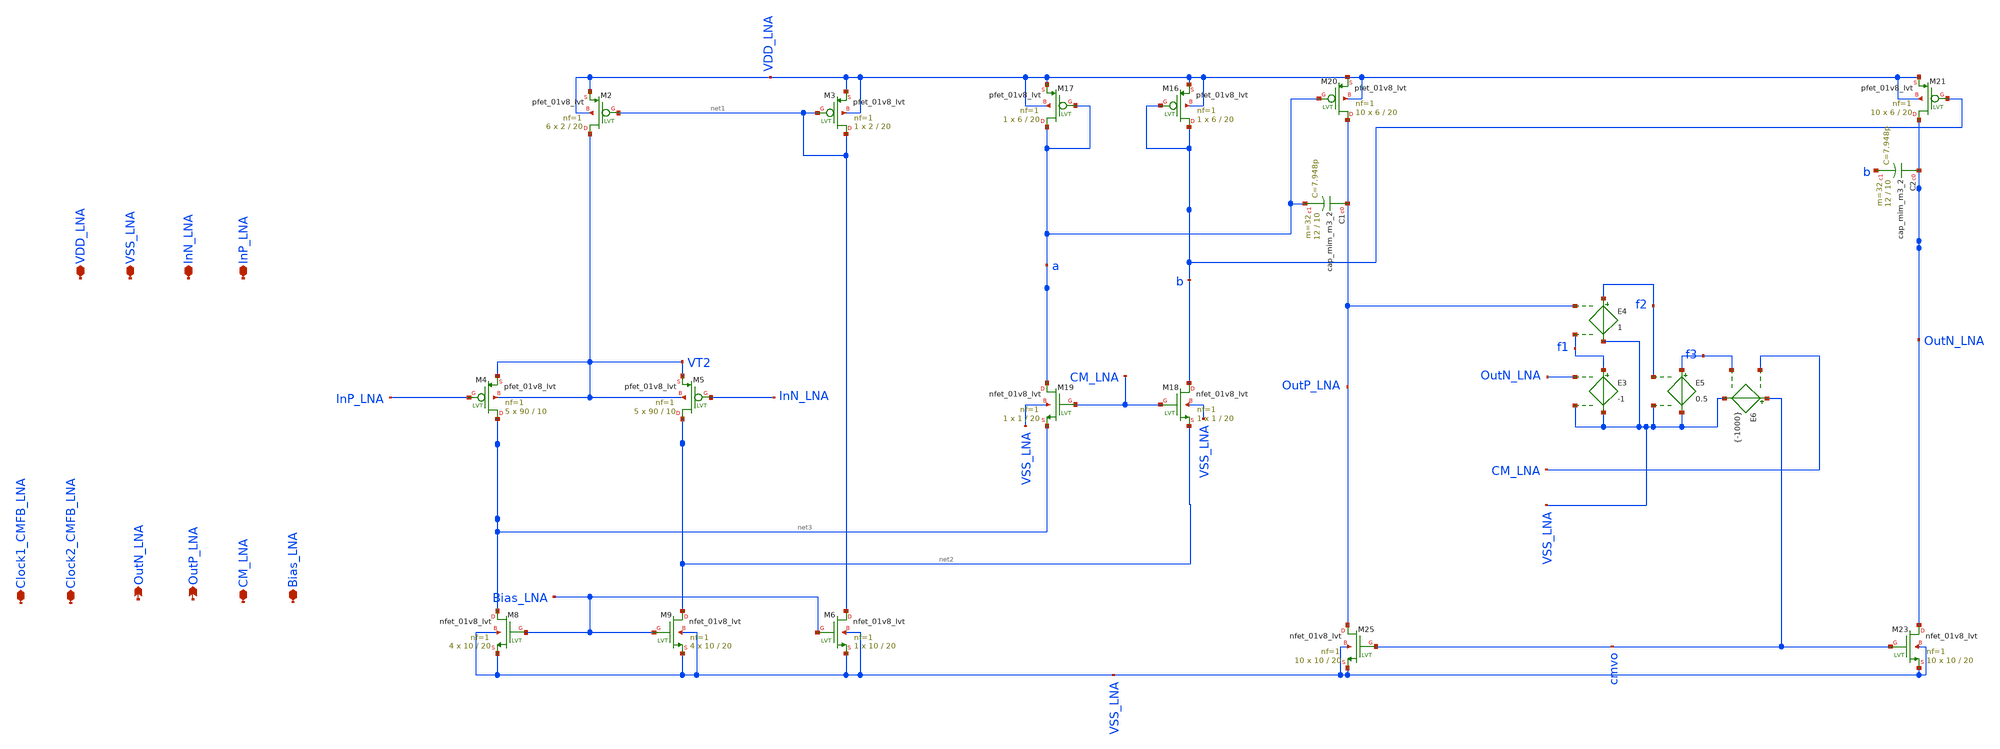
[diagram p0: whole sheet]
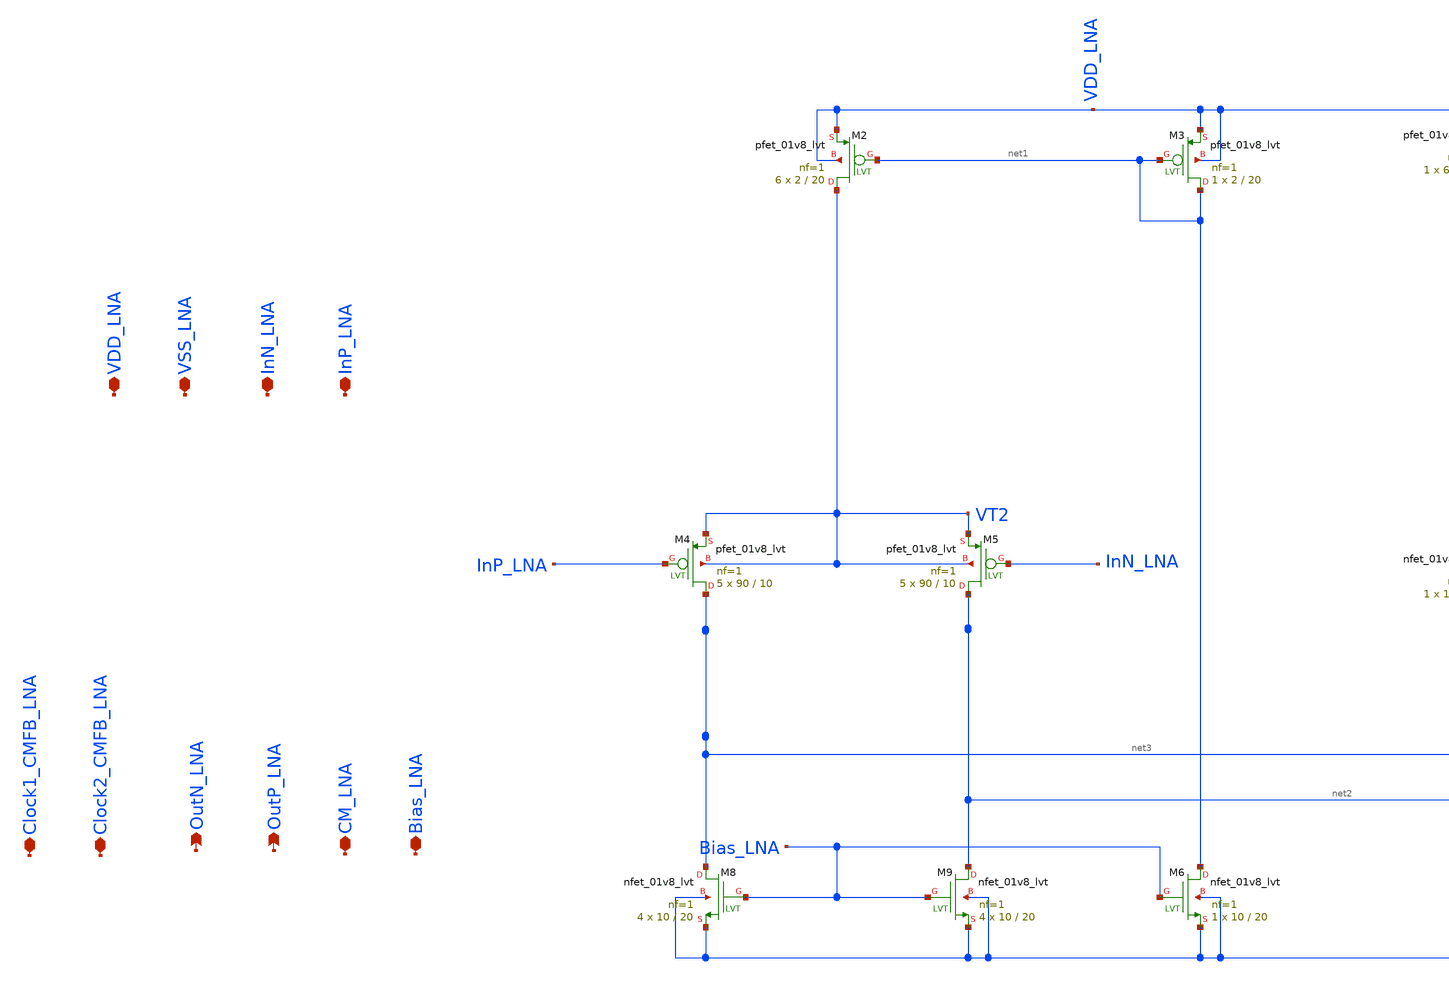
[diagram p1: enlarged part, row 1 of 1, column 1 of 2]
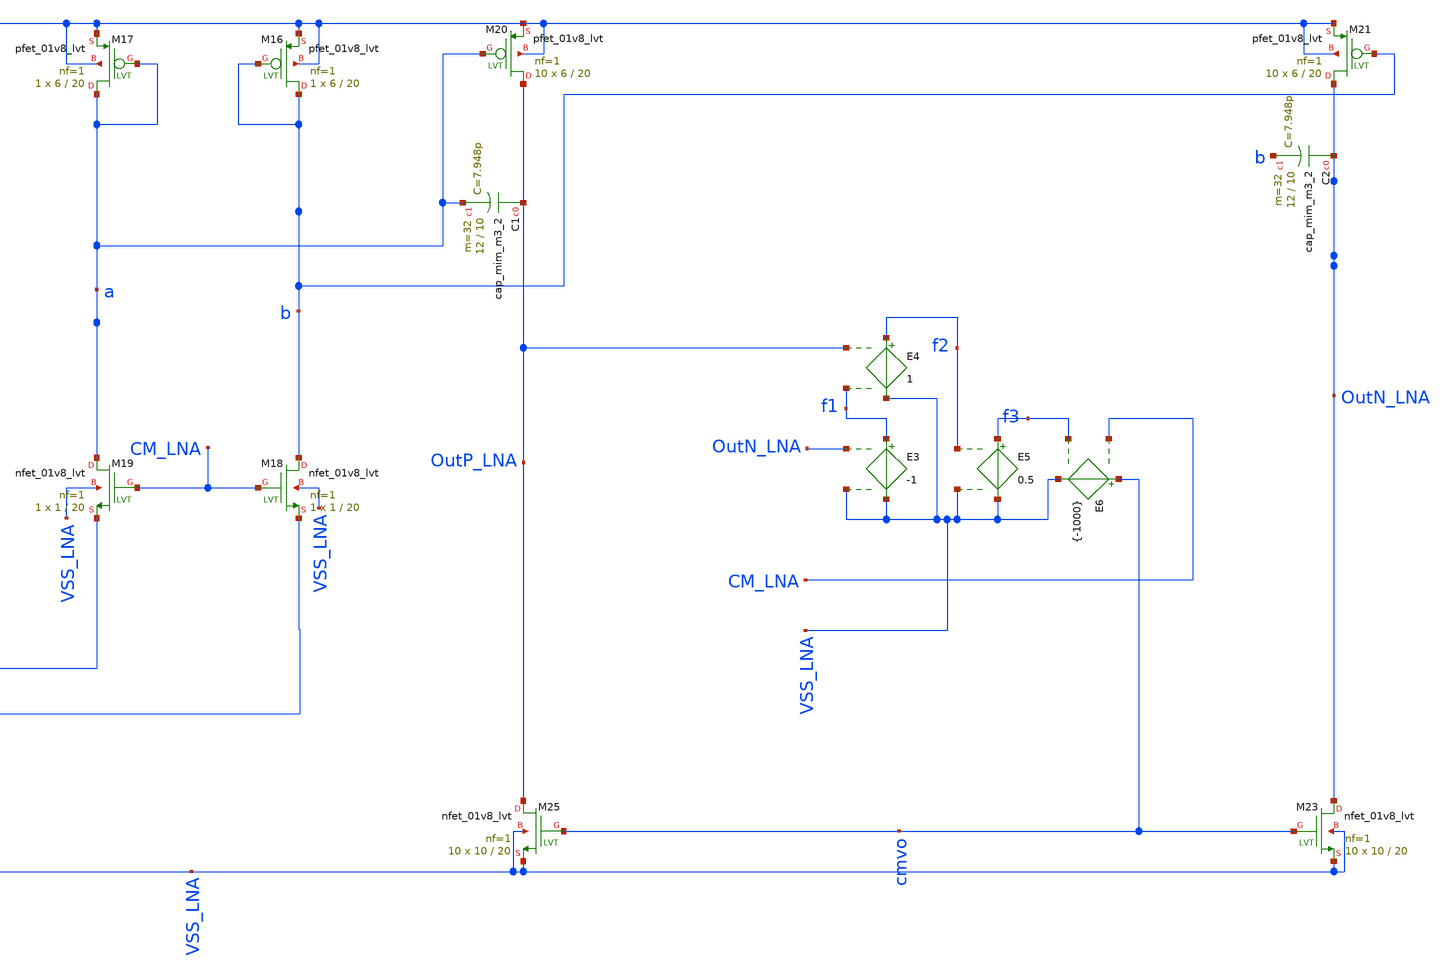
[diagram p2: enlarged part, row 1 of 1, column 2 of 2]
** sch_path: LNA_ac.sch
**.subckt LNA_ac InP_LNA InN_LNA VSS_LNA VDD_LNA CM_LNA OutP_LNA OutN_LNA Clock2_CMFB_LNA Bias_LNA
*+ Clock1_CMFB_LNA
*.iopin InP_LNA
*.iopin InN_LNA
*.iopin VSS_LNA
*.iopin VDD_LNA
*.iopin CM_LNA
*.opin OutP_LNA
*.opin OutN_LNA
*.iopin Clock2_CMFB_LNA
*.iopin Bias_LNA
*.iopin Clock1_CMFB_LNA
XM4 net3 InP_LNA VT2 VT2 sky130_fd_pr__pfet_01v8_lvt L=10 W=90 nf=1 ad='int((nf+1)/2) * W/nf * 0.29'
+ as='int((nf+2)/2) * W/nf * 0.29' pd='2*int((nf+1)/2) * (W/nf + 0.29)' ps='2*int((nf+2)/2) * (W/nf + 0.29)'
+ nrd='0.29 / W' nrs='0.29 / W' sa=0 sb=0 sd=0 mult=5 m=5
XM5 net2 InN_LNA VT2 VT2 sky130_fd_pr__pfet_01v8_lvt L=10 W=90 nf=1 ad='int((nf+1)/2) * W/nf * 0.29'
+ as='int((nf+2)/2) * W/nf * 0.29' pd='2*int((nf+1)/2) * (W/nf + 0.29)' ps='2*int((nf+2)/2) * (W/nf + 0.29)'
+ nrd='0.29 / W' nrs='0.29 / W' sa=0 sb=0 sd=0 mult=5 m=5
XM8 net3 Bias_LNA VSS_LNA VSS_LNA sky130_fd_pr__nfet_01v8_lvt L=20 W=10 nf=1 ad='int((nf+1)/2) * W/nf * 0.29'
+ as='int((nf+2)/2) * W/nf * 0.29' pd='2*int((nf+1)/2) * (W/nf + 0.29)' ps='2*int((nf+2)/2) * (W/nf + 0.29)'
+ nrd='0.29 / W' nrs='0.29 / W' sa=0 sb=0 sd=0 mult=4 m=4
XM9 net2 Bias_LNA VSS_LNA VSS_LNA sky130_fd_pr__nfet_01v8_lvt L=20 W=10 nf=1 ad='int((nf+1)/2) * W/nf * 0.29'
+ as='int((nf+2)/2) * W/nf * 0.29' pd='2*int((nf+1)/2) * (W/nf + 0.29)' ps='2*int((nf+2)/2) * (W/nf + 0.29)'
+ nrd='0.29 / W' nrs='0.29 / W' sa=0 sb=0 sd=0 mult=4 m=4
XM16 b b VDD_LNA VDD_LNA sky130_fd_pr__pfet_01v8_lvt L=20 W=6 nf=1 ad='int((nf+1)/2) * W/nf * 0.29' as='int((nf+2)/2) * W/nf * 0.29'
+ pd='2*int((nf+1)/2) * (W/nf + 0.29)' ps='2*int((nf+2)/2) * (W/nf + 0.29)' nrd='0.29 / W' nrs='0.29 / W'
+ sa=0 sb=0 sd=0 mult=1 m=1
XM17 a a VDD_LNA VDD_LNA sky130_fd_pr__pfet_01v8_lvt L=20 W=6 nf=1 ad='int((nf+1)/2) * W/nf * 0.29' as='int((nf+2)/2) * W/nf * 0.29'
+ pd='2*int((nf+1)/2) * (W/nf + 0.29)' ps='2*int((nf+2)/2) * (W/nf + 0.29)' nrd='0.29 / W' nrs='0.29 / W'
+ sa=0 sb=0 sd=0 mult=1 m=1
XM18 b CM_LNA net2 VSS_LNA sky130_fd_pr__nfet_01v8_lvt L=20 W=1 nf=1 ad='int((nf+1)/2) * W/nf * 0.29'
+ as='int((nf+2)/2) * W/nf * 0.29' pd='2*int((nf+1)/2) * (W/nf + 0.29)' ps='2*int((nf+2)/2) * (W/nf + 0.29)'
+ nrd='0.29 / W' nrs='0.29 / W' sa=0 sb=0 sd=0 mult=1 m=1
XM19 a CM_LNA net3 VSS_LNA sky130_fd_pr__nfet_01v8_lvt L=20 W=1 nf=1 ad='int((nf+1)/2) * W/nf * 0.29'
+ as='int((nf+2)/2) * W/nf * 0.29' pd='2*int((nf+1)/2) * (W/nf + 0.29)' ps='2*int((nf+2)/2) * (W/nf + 0.29)'
+ nrd='0.29 / W' nrs='0.29 / W' sa=0 sb=0 sd=0 mult=1 m=1
XM20 OutP_LNA a VDD_LNA VDD_LNA sky130_fd_pr__pfet_01v8_lvt L=20 W=6 nf=1 ad='int((nf+1)/2) * W/nf * 0.29'
+ as='int((nf+2)/2) * W/nf * 0.29' pd='2*int((nf+1)/2) * (W/nf + 0.29)' ps='2*int((nf+2)/2) * (W/nf + 0.29)'
+ nrd='0.29 / W' nrs='0.29 / W' sa=0 sb=0 sd=0 mult=10 m=10
XM21 OutN_LNA b VDD_LNA VDD_LNA sky130_fd_pr__pfet_01v8_lvt L=20 W=6 nf=1 ad='int((nf+1)/2) * W/nf * 0.29'
+ as='int((nf+2)/2) * W/nf * 0.29' pd='2*int((nf+1)/2) * (W/nf + 0.29)' ps='2*int((nf+2)/2) * (W/nf + 0.29)'
+ nrd='0.29 / W' nrs='0.29 / W' sa=0 sb=0 sd=0 mult=10 m=10
XM23 OutN_LNA cmvo VSS_LNA VSS_LNA sky130_fd_pr__nfet_01v8_lvt L=20 W=10 nf=1 ad='int((nf+1)/2) * W/nf * 0.29'
+ as='int((nf+2)/2) * W/nf * 0.29' pd='2*int((nf+1)/2) * (W/nf + 0.29)' ps='2*int((nf+2)/2) * (W/nf + 0.29)'
+ nrd='0.29 / W' nrs='0.29 / W' sa=0 sb=0 sd=0 mult=10 m=10
XM25 OutP_LNA cmvo VSS_LNA VSS_LNA sky130_fd_pr__nfet_01v8_lvt L=20 W=10 nf=1 ad='int((nf+1)/2) * W/nf * 0.29'
+ as='int((nf+2)/2) * W/nf * 0.29' pd='2*int((nf+1)/2) * (W/nf + 0.29)' ps='2*int((nf+2)/2) * (W/nf + 0.29)'
+ nrd='0.29 / W' nrs='0.29 / W' sa=0 sb=0 sd=0 mult=10 m=10
XM2 VT2 net1 VDD_LNA VDD_LNA sky130_fd_pr__pfet_01v8_lvt L=20 W=2 nf=1 ad='int((nf+1)/2) * W/nf * 0.29'
+ as='int((nf+2)/2) * W/nf * 0.29' pd='2*int((nf+1)/2) * (W/nf + 0.29)' ps='2*int((nf+2)/2) * (W/nf + 0.29)'
+ nrd='0.29 / W' nrs='0.29 / W' sa=0 sb=0 sd=0 mult=6 m=6
XM3 net1 net1 VDD_LNA VDD_LNA sky130_fd_pr__pfet_01v8_lvt L=20 W=2 nf=1 ad='int((nf+1)/2) * W/nf * 0.29'
+ as='int((nf+2)/2) * W/nf * 0.29' pd='2*int((nf+1)/2) * (W/nf + 0.29)' ps='2*int((nf+2)/2) * (W/nf + 0.29)'
+ nrd='0.29 / W' nrs='0.29 / W' sa=0 sb=0 sd=0 mult=1 m=1
XM6 net1 Bias_LNA VSS_LNA VSS_LNA sky130_fd_pr__nfet_01v8_lvt L=20 W=10 nf=1 ad='int((nf+1)/2) * W/nf * 0.29'
+ as='int((nf+2)/2) * W/nf * 0.29' pd='2*int((nf+1)/2) * (W/nf + 0.29)' ps='2*int((nf+2)/2) * (W/nf + 0.29)'
+ nrd='0.29 / W' nrs='0.29 / W' sa=0 sb=0 sd=0 mult=1 m=1
E3 f1 VSS_LNA OutN_LNA VSS_LNA -1
E4 f2 VSS_LNA OutP_LNA f1 1
E5 f3 VSS_LNA f2 VSS_LNA 0.5
E6 cmvo VSS_LNA CM_LNA f3 {-1000}
XC1 OutP_LNA a sky130_fd_pr__cap_mim_m3_2 W=12 L=10 MF=32 m=32
XC2 OutN_LNA b sky130_fd_pr__cap_mim_m3_2 W=12 L=10 MF=32 m=32
**.ends
.end
